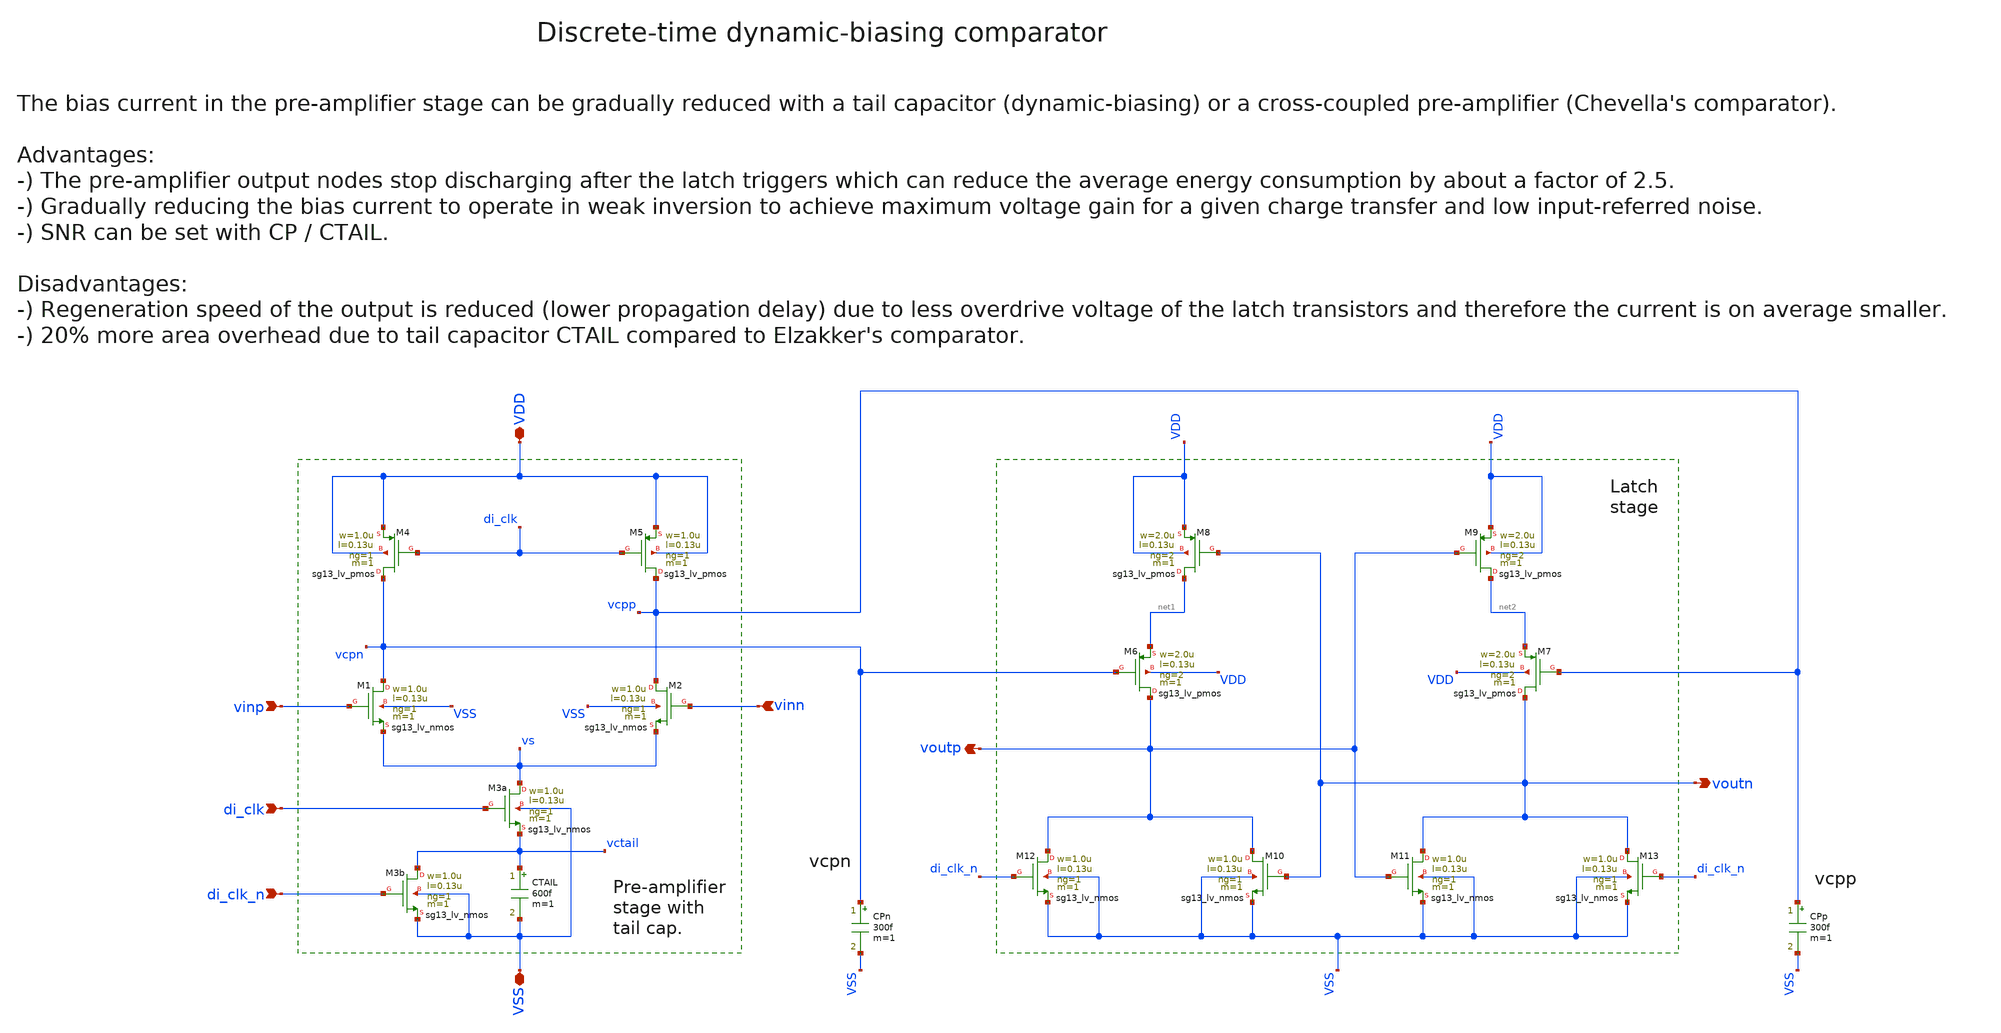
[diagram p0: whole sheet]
** sch_path: SG13G2_ATBS-ADC-main/xschem/comparator/discrete_time/Dynamic-biasing/dynamic_biasing_comparator.sch
**.subckt dynamic_biasing_comparator VDD voutp voutn di_clk_n VSS vinp vinn di_clk
*.iopin VDD
*.opin voutp
*.opin voutn
*.ipin di_clk_n
*.iopin VSS
*.ipin vinp
*.ipin vinn
*.ipin di_clk
XM3a vs di_clk vctail VSS sg13_lv_nmos w=1.0u l=0.13u ng=1 m=1 mm_ok=1
XM12 voutp di_clk_n VSS VSS sg13_lv_nmos w=1.0u l=0.13u ng=1 m=1 mm_ok=1
XM8 net1 voutn VDD VDD sg13_lv_pmos w=2.0u l=0.13u ng=2 m=1 mm_ok=1
XM10 voutp voutn VSS VSS sg13_lv_nmos w=1.0u l=0.13u ng=1 m=1 mm_ok=1
XM11 voutn voutp VSS VSS sg13_lv_nmos w=1.0u l=0.13u ng=1 m=1 mm_ok=1
XM13 voutn di_clk_n VSS VSS sg13_lv_nmos w=1.0u l=0.13u ng=1 m=1 mm_ok=1
CPn vcpn VSS 300f m=1
CPp vcpp VSS 300f m=1
XM9 net2 voutp VDD VDD sg13_lv_pmos w=2.0u l=0.13u ng=2 m=1 mm_ok=1
XM6 voutp vcpn net1 VDD sg13_lv_pmos w=2.0u l=0.13u ng=2 m=1 mm_ok=1
XM7 voutn vcpp net2 VDD sg13_lv_pmos w=2.0u l=0.13u ng=2 m=1 mm_ok=1
CTAIL vctail VSS 600f m=1
XM3b vctail di_clk_n VSS VSS sg13_lv_nmos w=1.0u l=0.13u ng=1 m=1 mm_ok=1
XM1 vcpn vinp vs VSS sg13_lv_nmos w=1.0u l=0.13u ng=1 m=1 mm_ok=1
XM2 vcpp vinn vs VSS sg13_lv_nmos w=1.0u l=0.13u ng=1 m=1 mm_ok=1
XM4 vcpn di_clk VDD VDD sg13_lv_pmos w=1.0u l=0.13u ng=1 m=1 mm_ok=1
XM5 vcpp di_clk VDD VDD sg13_lv_pmos w=1.0u l=0.13u ng=1 m=1 mm_ok=1
**.ends
.end
